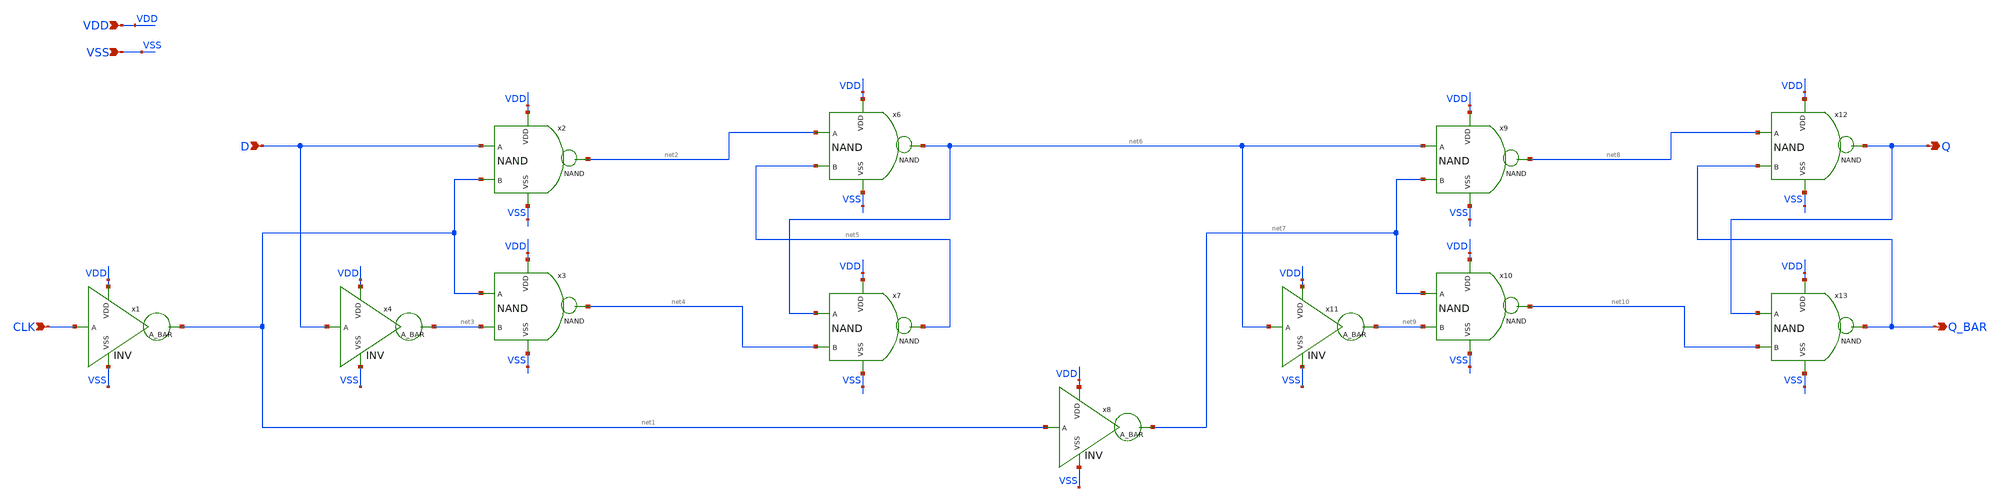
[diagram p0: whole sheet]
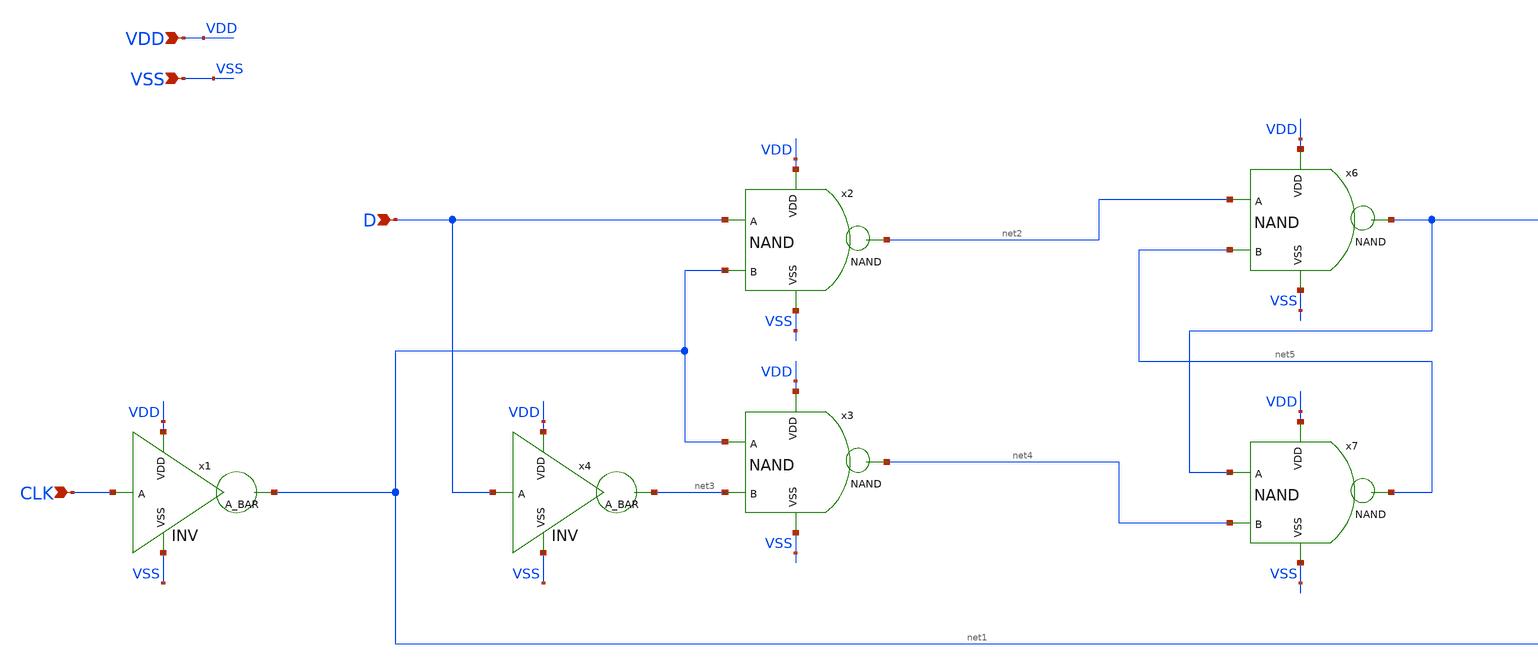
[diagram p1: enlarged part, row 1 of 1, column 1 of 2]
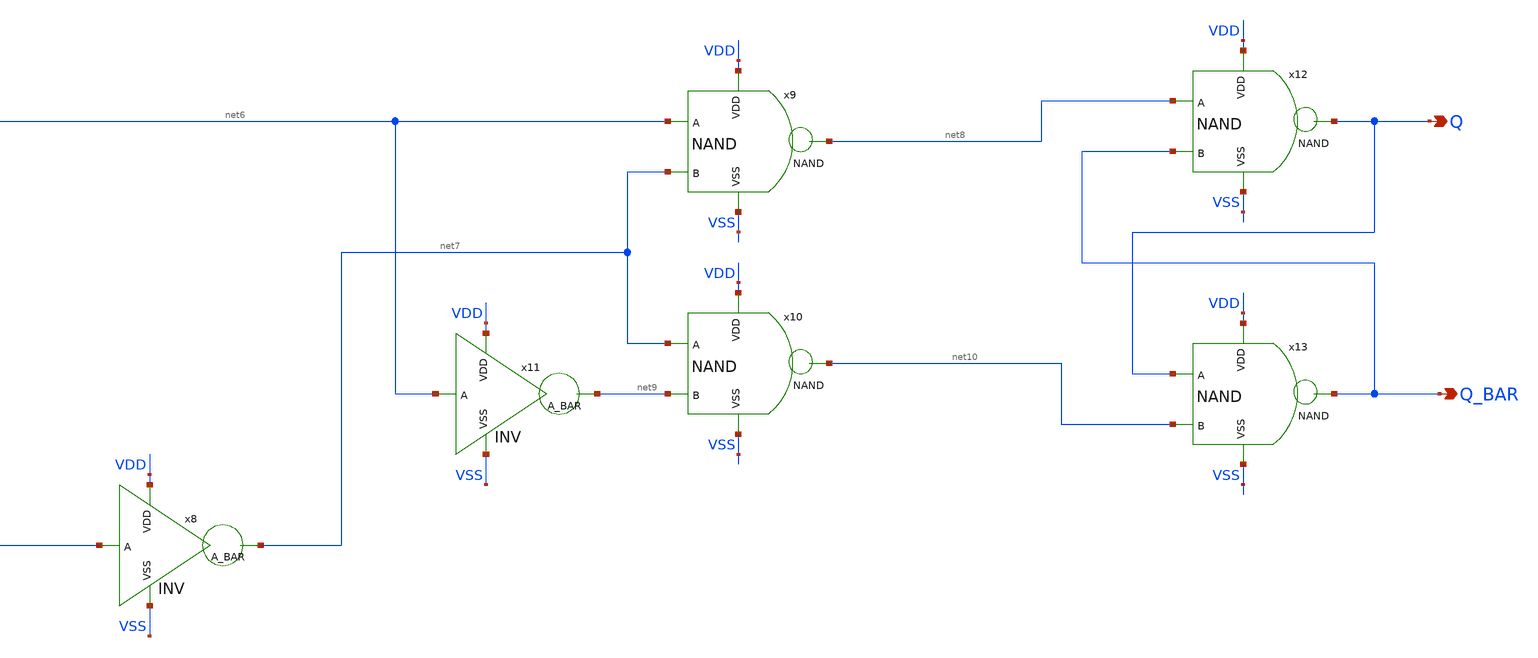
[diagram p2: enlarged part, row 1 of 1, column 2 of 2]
** sch_path: designs/libs/qw_core_analog/DFF2_3v3.sch
**.subckt DFF2_3v3 VDD VSS D CLK Q Q_BAR
*.ipin VDD
*.ipin VSS
*.ipin D
*.ipin CLK
*.opin Q
*.opin Q_BAR
x1 VDD CLK net1 VSS INV
x2 VDD net2 D net1 VSS NAND
x3 VDD net4 net1 net3 VSS NAND
x4 VDD D net3 VSS INV
x6 VDD net6 net2 net5 VSS NAND
x7 VDD net5 net6 net4 VSS NAND
x8 VDD net1 net7 VSS INV
x9 VDD net8 net6 net7 VSS NAND
x10 VDD net10 net7 net9 VSS NAND
x11 VDD net6 net9 VSS INV
x12 VDD Q net8 Q_BAR VSS NAND
x13 VDD Q_BAR Q net10 VSS NAND
**.ends
.end
